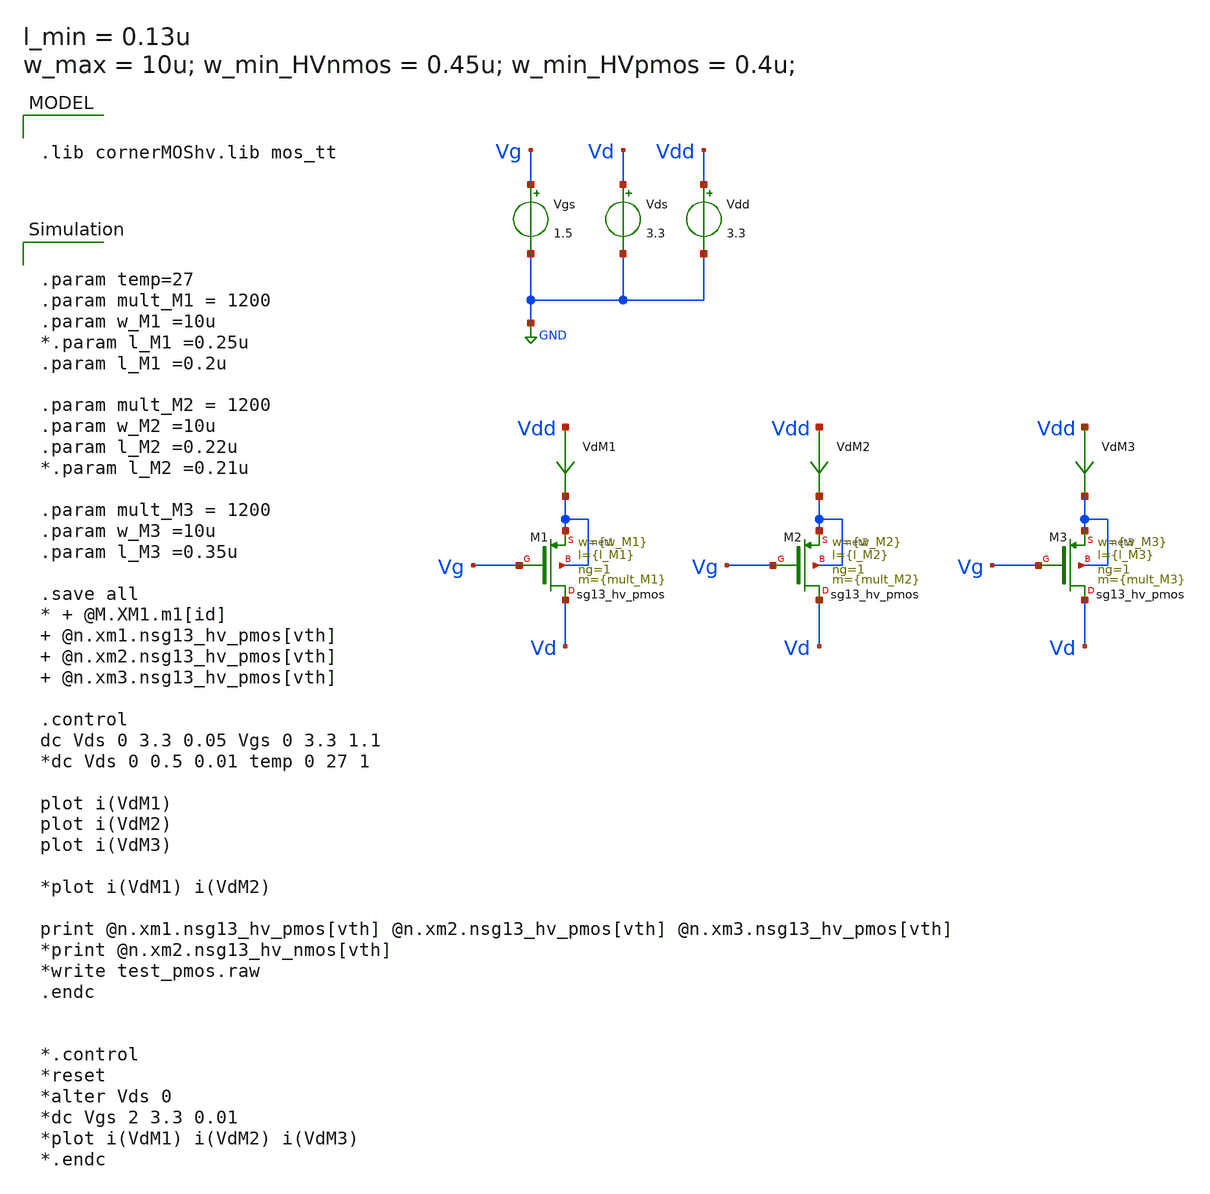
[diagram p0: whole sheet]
** sch_path: xschem/TB_hvPMOS_charact_v1p2.sch
**.subckt TB_hvPMOS_charact_v1p2
XM1 Vd Vg net1 net1 sg13_hv_pmos w={w_M1} l={l_M1} ng=1 m={mult_M1} mm_ok=1
Vgs Vg GND 1.5
Vds Vd GND 3.3
Vdd Vdd GND 3.3
VdM1 Vdd net1 0
.save i(vdm1)
XM2 Vd Vg net2 net2 sg13_hv_pmos w={w_M2} l={l_M2} ng=1 m={mult_M2} mm_ok=1
VdM2 Vdd net2 0
.save i(vdm2)
XM3 Vd Vg net3 net3 sg13_hv_pmos w={w_M3} l={l_M3} ng=1 m={mult_M3} mm_ok=1
VdM3 Vdd net3 0
.save i(vdm3)
**** begin user architecture code


.param temp=27
.param mult_M1 = 1200
.param w_M1 =10u
*.param l_M1 =0.25u
.param l_M1 =0.2u

.param mult_M2 = 1200
.param w_M2 =10u
.param l_M2 =0.22u
*.param l_M2 =0.21u

.param mult_M3 = 1200
.param w_M3 =10u
.param l_M3 =0.35u

.save all
* + @M.XM1.m1[id]  @n.xm1.nsg13_hv_pmos[vth]  @n.xm2.nsg13_hv_pmos[vth]  @n.xm3.nsg13_hv_pmos[vth]

.control
dc Vds 0 3.3 0.05 Vgs 0 3.3 1.1
*dc Vds 0 0.5 0.01 temp 0 27 1

plot i(VdM1)
plot i(VdM2)
plot i(VdM3)

*plot i(VdM1) i(VdM2)

print @n.xm1.nsg13_hv_pmos[vth] @n.xm2.nsg13_hv_pmos[vth] @n.xm3.nsg13_hv_pmos[vth]
*print @n.xm2.nsg13_hv_nmos[vth]
*write test_pmos.raw
.endc


*.control
*reset
*alter Vds 0
*dc Vgs 2 3.3 0.01
*plot i(VdM1) i(VdM2) i(VdM3)
*.endc




.lib cornerMOShv.lib mos_tt

**** end user architecture code
**.ends
.GLOBAL GND
.end
